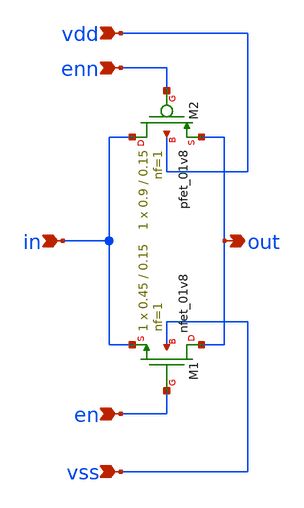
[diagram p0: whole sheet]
** sch_path: xschem/tg.sch
**.subckt tg vdd enn in en vss out
*.ipin vdd
*.ipin enn
*.ipin in
*.ipin en
*.ipin vss
*.opin out
XM1 out en in vss sky130_fd_pr__nfet_01v8 L=0.15 W=0.45 nf=1 ad='int((nf+1)/2) * W/nf * 0.29' as='int((nf+2)/2) * W/nf * 0.29'
+ pd='2*int((nf+1)/2) * (W/nf + 0.29)' ps='2*int((nf+2)/2) * (W/nf + 0.29)' nrd='0.29 / W' nrs='0.29 / W'
+ sa=0 sb=0 sd=0 mult=1 m=1
XM2 in enn out vdd sky130_fd_pr__pfet_01v8 L=0.15 W=0.9 nf=1 ad='int((nf+1)/2) * W/nf * 0.29' as='int((nf+2)/2) * W/nf * 0.29'
+ pd='2*int((nf+1)/2) * (W/nf + 0.29)' ps='2*int((nf+2)/2) * (W/nf + 0.29)' nrd='0.29 / W' nrs='0.29 / W'
+ sa=0 sb=0 sd=0 mult=1 m=1
**.ends
.end
